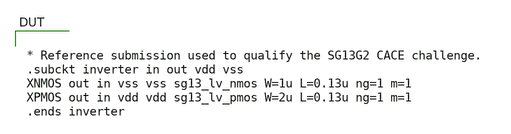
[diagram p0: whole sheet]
** sch_path: challenges/demo-cmos-inverter/xschem/inverter.sch
**.subckt inverter
**** begin user architecture code


* Reference submission used to qualify the SG13G2 CACE challenge.
.subckt inverter in out vdd vss
XNMOS out in vss vss sg13_lv_nmos W=1u L=0.13u ng=1 m=1
XPMOS out in vdd vdd sg13_lv_pmos W=2u L=0.13u ng=1 m=1
.ends inverter


**** end user architecture code
**.ends
.end
